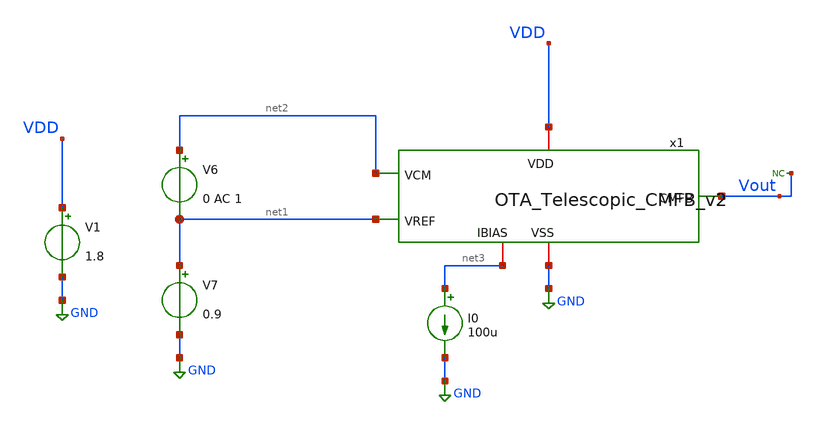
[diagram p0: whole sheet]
** sch_path: Differential_OTA_Telescopic_IHP/OTA_Telescopic_CMFB_v2_TB.sch
**.subckt OTA_Telescopic_CMFB_v2_TB
I0 net3 GND 100u
V1 VDD GND 1.8
V6 net2 net1 0 AC 1
V7 net1 GND 0.9
* noconn Vout
x1 VDD net3 Vout net1 net2 GND OTA_Telescopic_CMFB_v2
**** begin user architecture code

** opencircuitdesign pdks install
.lib $::SKYWATER_MODELS/sky130.lib.spice tt




.control
save all

* AC simulation
ac dec 10 1 1T
let Av = db(v(Vout))
meas ac Ao MAX Av
let ABW = Ao-3
meas ac BW WHEN Av=ABW
meas ac UGBW WHEN Av=0
let phase_vec = 180/pi*cph(v(Vout))

* Phase margin (PM)
meas ac phase FIND phase_vec WHEN frequency=UGBW
let PM = phase+180
print PM

* Gain margin (GM)
meas ac freq180 FIND frequency WHEN phase_vec=-180
meas ac gain FIND Av WHEN frequency=freq180
let GM = 0-gain
print GM
plot Av
plot phase_vec


*DC simulation

op
let vout_dc = v(Vout1)
print vout_dc
write OTA_Telescopic_CMFB_v2_TB.raw

.endc




.op

.save all

.save @m.x1.xm0.msky130_fd_pr__pfet_01v8_lvt[id]
.save @m.x1.xm0.msky130_fd_pr__pfet_01v8_lvt[gm]
.save @m.x1.xm1.msky130_fd_pr__pfet_01v8_lvt[id]
.save @m.x1.xm1.msky130_fd_pr__pfet_01v8_lvt[gm]
.save @m.x1.xm2.msky130_fd_pr__pfet_01v8_lvt[id]
.save @m.x1.xm2.msky130_fd_pr__pfet_01v8_lvt[gm]

.save @m.x1.xm3.msky130_fd_pr__nfet_01v8_lvt[id]
.save @m.x1.xm3.msky130_fd_pr__nfet_01v8_lvt[gm]
.save @m.x1.xm4.msky130_fd_pr__nfet_01v8_lvt[id]
.save @m.x1.xm4.msky130_fd_pr__nfet_01v8_lvt[gm]

.save @m.x1.xm5.msky130_fd_pr__pfet_01v8_lvt[id]
.save @m.x1.xm5.msky130_fd_pr__pfet_01v8_lvt[gm]

.control

*let vdssat_M1 = @m.x1.xm1.msky130_fd_pr__nfet_01v8_lvt[vdsat]
*let vdssat_M3 = @m.x1.xm3.msky130_fd_pr__nfet_01v8_lvt[vdsat]
*let vdssat_M5 = @m.x1.xm5.msky130_fd_pr__pfet_01v8_lvt[vdsat]
*let vdssat_M7 = @m.x1.xm7.msky130_fd_pr__pfet_01v8_lvt[vdsat]
*let vdssat_M0 = @m.x1.xm0.msky130_fd_pr__nfet_01v8_lvt[vdsat]

*print vdssat_M1
*print vdssat_M3
*print vdssat_M5
*print vdssat_M7
*print vdssat_M0

.endc



**** end user architecture code
**.ends

* expanding   symbol:  OTA_Telescopic_CMFB_v2.sym # of pins=6
** sym_path: Differential_OTA_Telescopic_IHP/OTA_Telescopic_CMFB_v2.sym
** sch_path: Differential_OTA_Telescopic_IHP/OTA_Telescopic_CMFB_v2.sch
.subckt OTA_Telescopic_CMFB_v2 VDD IBIAS CMFB VREF VCM VSS
*.iopin VDD
*.iopin IBIAS
*.iopin VSS
*.ipin VREF
*.ipin VCM
*.opin CMFB
XM0 VP IBIAS VDD VDD sky130_fd_pr__pfet_01v8_lvt L=0.75 W=5 nf=1 ad='int((nf+1)/2) * W/nf * 0.29' as='int((nf+2)/2) * W/nf * 0.29'
+ pd='2*int((nf+1)/2) * (W/nf + 0.29)' ps='2*int((nf+2)/2) * (W/nf + 0.29)' nrd='0.29 / W' nrs='0.29 / W'
+ sa=0 sb=0 sd=0 mult=2*5 m=2*5
XM1 net1 VREF VP VDD sky130_fd_pr__pfet_01v8_lvt L=0.35 W=10 nf=1 ad='int((nf+1)/2) * W/nf * 0.29' as='int((nf+2)/2) * W/nf * 0.29'
+ pd='2*int((nf+1)/2) * (W/nf + 0.29)' ps='2*int((nf+2)/2) * (W/nf + 0.29)' nrd='0.29 / W' nrs='0.29 / W'
+ sa=0 sb=0 sd=0 mult=40 m=40
XM2 CMFB VCM VP VDD sky130_fd_pr__pfet_01v8_lvt L=0.35 W=10 nf=1 ad='int((nf+1)/2) * W/nf * 0.29' as='int((nf+2)/2) * W/nf * 0.29'
+ pd='2*int((nf+1)/2) * (W/nf + 0.29)' ps='2*int((nf+2)/2) * (W/nf + 0.29)' nrd='0.29 / W' nrs='0.29 / W'
+ sa=0 sb=0 sd=0 mult=40 m=40
XM5 IBIAS IBIAS VDD VDD sky130_fd_pr__pfet_01v8_lvt L=0.75 W=5 nf=1 ad='int((nf+1)/2) * W/nf * 0.29'
+ as='int((nf+2)/2) * W/nf * 0.29' pd='2*int((nf+1)/2) * (W/nf + 0.29)' ps='2*int((nf+2)/2) * (W/nf + 0.29)'
+ nrd='0.29 / W' nrs='0.29 / W' sa=0 sb=0 sd=0 mult=5 m=5
XM3 net1 net1 VSS VSS sky130_fd_pr__nfet_01v8_lvt L=0.6 W=65 nf=1 ad='int((nf+1)/2) * W/nf * 0.29' as='int((nf+2)/2) * W/nf * 0.29'
+ pd='2*int((nf+1)/2) * (W/nf + 0.29)' ps='2*int((nf+2)/2) * (W/nf + 0.29)' nrd='0.29 / W' nrs='0.29 / W'
+ sa=0 sb=0 sd=0 mult=2 m=2
XM4 CMFB CMFB VSS VSS sky130_fd_pr__nfet_01v8_lvt L=0.6 W=65 nf=1 ad='int((nf+1)/2) * W/nf * 0.29' as='int((nf+2)/2) * W/nf * 0.29'
+ pd='2*int((nf+1)/2) * (W/nf + 0.29)' ps='2*int((nf+2)/2) * (W/nf + 0.29)' nrd='0.29 / W' nrs='0.29 / W'
+ sa=0 sb=0 sd=0 mult=2 m=2
.ends

.GLOBAL GND
.end
